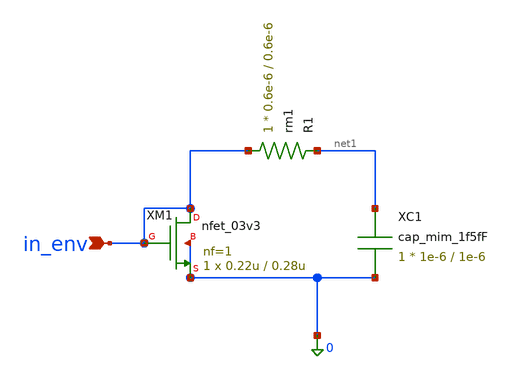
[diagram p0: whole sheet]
** sch_path: analog/B04_envelope.sch
**.subckt B04_envelope in_env
*.ipin in_env
XM1 in_env in_env 0 0 nfet_03v3 L=0.28u W=0.22u nf=1 ad='int((nf+1)/2) * W/nf * 0.18u' as='int((nf+2)/2) * W/nf * 0.18u'
+ pd='2*int((nf+1)/2) * (W/nf + 0.18u)' ps='2*int((nf+2)/2) * (W/nf + 0.18u)' nrd='0.18u / W' nrs='0.18u / W'
+ sa=0 sb=0 sd=0 m=1
XR1 in_env net1 rm1 r_width=0.6e-6 r_length=0.6e-6 m=1
XC1 net1 0 cap_mim_1f5fF c_width=1e-6 c_length=1e-6 m=1
**** begin user architecture code

.include /foss/pdks/ciel/gf180mcu/versions/7b70722e33c03fcb5dabcf4d479fb0822d9251c9/gf180mcuD/libs.tech/ngspice/design.ngspice
.lib /foss/pdks/ciel/gf180mcu/versions/7b70722e33c03fcb5dabcf4d479fb0822d9251c9/gf180mcuD/libs.tech/ngspice/sm141064.ngspice typical

**** end user architecture code
**.ends
.end
